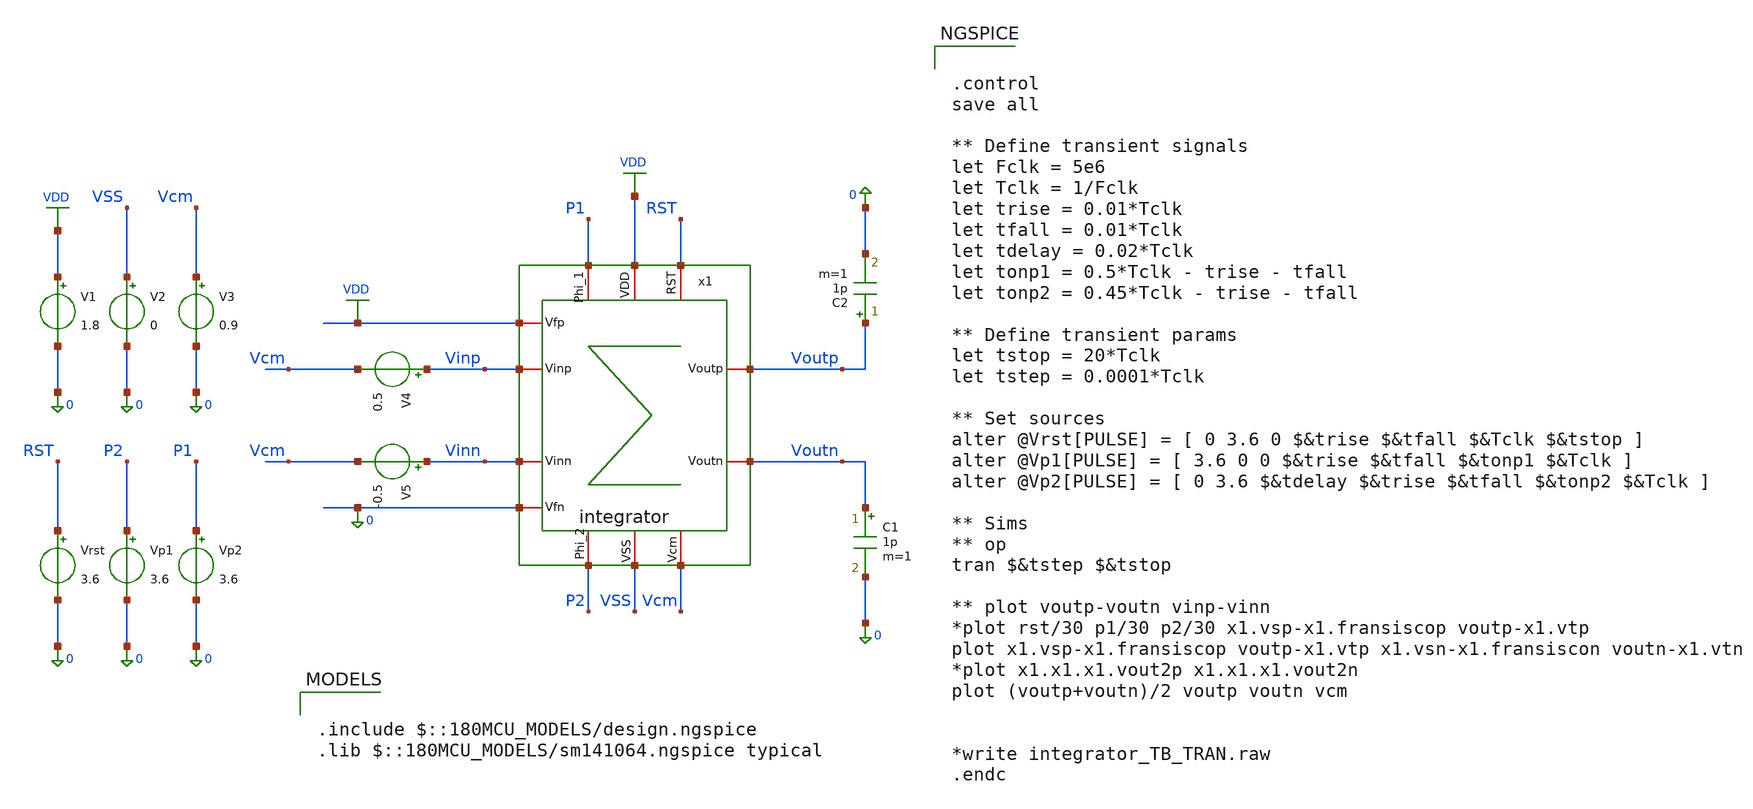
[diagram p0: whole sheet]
** sch_path: designs/DS_modulator/integrator/xschem/integrator_TB_TRAN.sch
**.subckt integrator_TB_TRAN
V1 VDD 0 1.8
V2 VSS 0 0
V3 Vcm 0 0.9
V4 Vinp Vcm 0.5
V5 Vinn Vcm -0.5
Vrst RST 0 3.6
Vp1 P2 0 3.6
Vp2 P1 0 3.6
C1 Voutn 0 1p m=1
C2 Voutp 0 1p m=1
x1 RST Vinp VDD P1 Voutp Vcm Voutn P2 VSS Vinn VDD 0 integrator
**** begin user architecture code

.include $::180MCU_MODELS/design.ngspice
.lib $::180MCU_MODELS/sm141064.ngspice typical



.control
save all

** Define transient signals
let Fclk = 5e6
let Tclk = 1/Fclk
let trise = 0.01*Tclk
let tfall = 0.01*Tclk
let tdelay = 0.02*Tclk
let tonp1 = 0.5*Tclk - trise - tfall
let tonp2 = 0.45*Tclk - trise - tfall

** Define transient params
let tstop = 20*Tclk
let tstep = 0.0001*Tclk

** Set sources
alter @Vrst[PULSE] = [ 0 3.6 0 $&trise $&tfall $&Tclk $&tstop ]
alter @Vp1[PULSE] = [ 3.6 0 0 $&trise $&tfall $&tonp1 $&Tclk ]
alter @Vp2[PULSE] = [ 0 3.6 $&tdelay $&trise $&tfall $&tonp2 $&Tclk ]

** Sims
** op
tran $&tstep $&tstop

** plot voutp-voutn vinp-vinn
*plot rst/30 p1/30 p2/30 x1.vsp-x1.fransiscop voutp-x1.vtp
plot x1.vsp-x1.fransiscop voutp-x1.vtp x1.vsn-x1.fransiscon voutn-x1.vtn
*plot x1.x1.x1.vout2p x1.x1.x1.vout2n
plot (voutp+voutn)/2 voutp voutn vcm


*write integrator_TB_TRAN.raw
.endc


**** end user architecture code
**.ends
.GLOBAL VDD
.end
